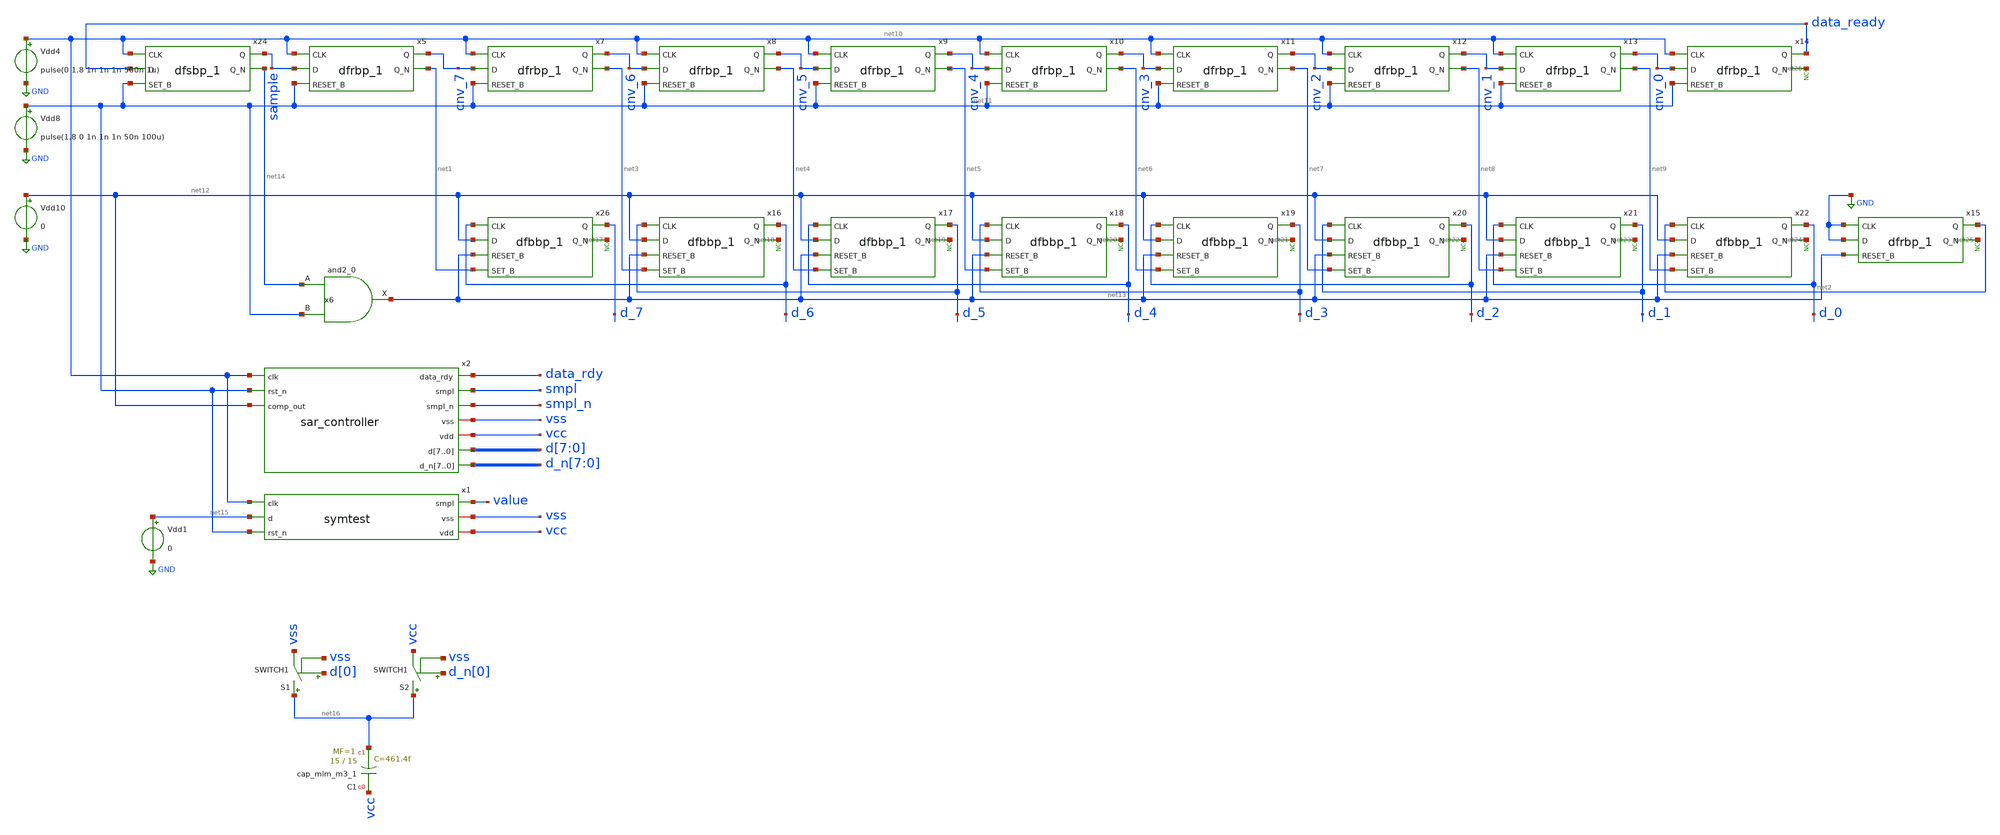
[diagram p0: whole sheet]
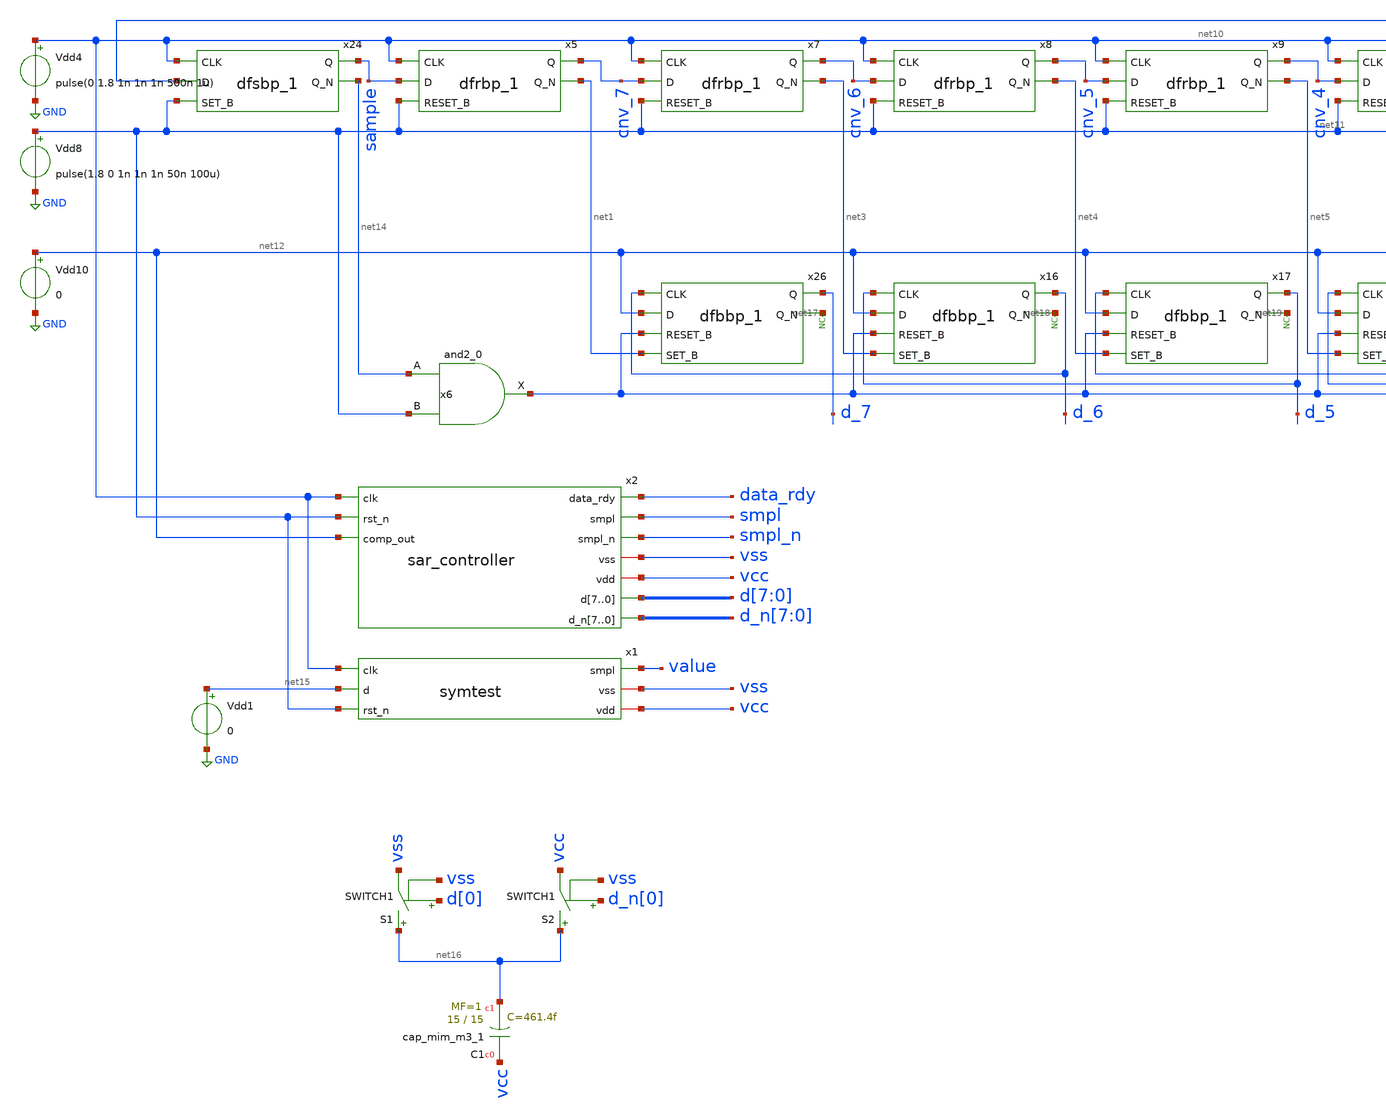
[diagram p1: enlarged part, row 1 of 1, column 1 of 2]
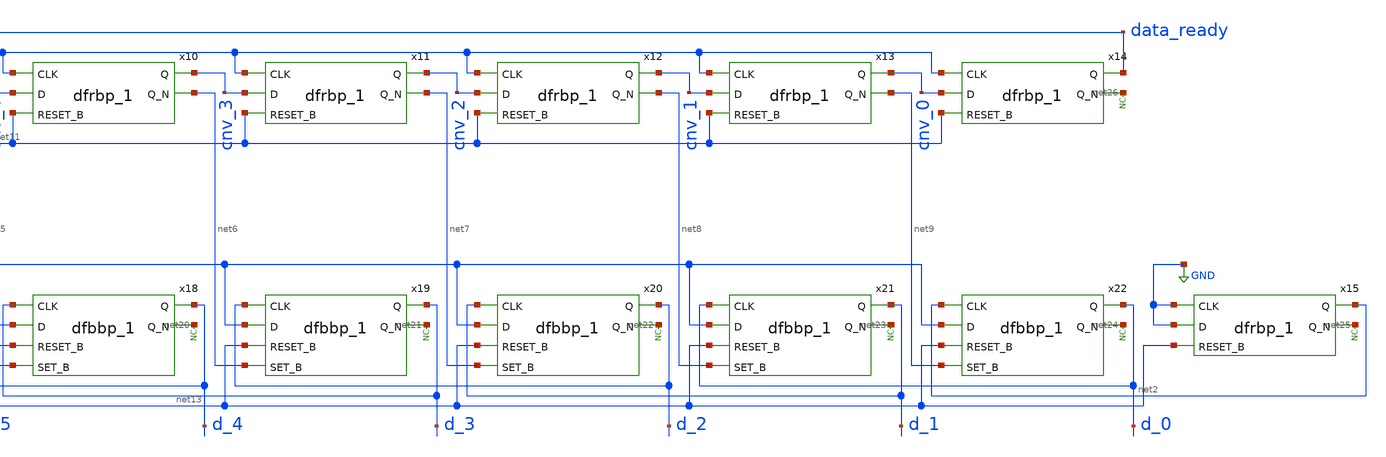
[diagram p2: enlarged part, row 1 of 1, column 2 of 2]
** sch_path: test/testbench/controller_tb.sch
.lib $::SKYWATER_MODELS/sky130.lib.spice tt
.include $::SKYWATER_STDCELLS/sky130_fd_sc_hd.spice

**.subckt controller_tb
x26 d_6 net12 net13 net1 vss vss vcc vcc d_7 net17 sky130_fd_sc_hd__dfbbp_1
x16 d_5 net12 net13 net3 vss vss vcc vcc d_6 net18 sky130_fd_sc_hd__dfbbp_1
x17 d_4 net12 net13 net4 vss vss vcc vcc d_5 net19 sky130_fd_sc_hd__dfbbp_1
x18 d_3 net12 net13 net5 vss vss vcc vcc d_4 net20 sky130_fd_sc_hd__dfbbp_1
x19 d_2 net12 net13 net6 vss vss vcc vcc d_3 net21 sky130_fd_sc_hd__dfbbp_1
x20 d_1 net12 net13 net7 vss vss vcc vcc d_2 net22 sky130_fd_sc_hd__dfbbp_1
x21 d_0 net12 net13 net8 vss vss vcc vcc d_1 net23 sky130_fd_sc_hd__dfbbp_1
x22 net2 net12 net13 net9 vss vss vcc vcc d_0 net24 sky130_fd_sc_hd__dfbbp_1
x5 net10 sample net11 vss vss vcc vcc cnv_7 net1 sky130_fd_sc_hd__dfrbp_1
Vdd10 net12 GND 0
Vdd8 net11 GND pulse(1.8 0 1n 1n 1n 50n 100u)
Vdd4 net10 GND pulse(0 1.8 1n 1n 1n 500n 1u)
* noconn #net17
* noconn #net18
* noconn #net19
* noconn #net20
* noconn #net21
* noconn #net22
* noconn #net23
* noconn #net24
* noconn #net25
x7 net10 cnv_7 net11 vss vss vcc vcc cnv_6 net3 sky130_fd_sc_hd__dfrbp_1
x8 net10 cnv_6 net11 vss vss vcc vcc cnv_5 net4 sky130_fd_sc_hd__dfrbp_1
x9 net10 cnv_5 net11 vss vss vcc vcc cnv_4 net5 sky130_fd_sc_hd__dfrbp_1
x10 net10 cnv_4 net11 vss vss vcc vcc cnv_3 net6 sky130_fd_sc_hd__dfrbp_1
x11 net10 cnv_3 net11 vss vss vcc vcc cnv_2 net7 sky130_fd_sc_hd__dfrbp_1
x12 net10 cnv_2 net11 vss vss vcc vcc cnv_1 net8 sky130_fd_sc_hd__dfrbp_1
x13 net10 cnv_1 net11 vss vss vcc vcc cnv_0 net9 sky130_fd_sc_hd__dfrbp_1
x14 net10 cnv_0 net11 vss vss vcc vcc data_ready net26 sky130_fd_sc_hd__dfrbp_1
* noconn #net26
x15 GND GND net13 vss vss vcc vcc net2 net25 sky130_fd_sc_hd__dfrbp_1
x24 net10 data_ready net11 vss vss vcc vcc sample net14 sky130_fd_sc_hd__dfsbp_1
x6 net14 net11 vss vss vcc vcc net13 sky130_fd_sc_hd__and2_0
x1 net10 value net15 net11 vss vcc symtest
Vdd1 net15 GND 0
x2 net10 data_rdy smpl net11 smpl_n net12 vss vcc d[7] d[6] d[5] d[4] d[3] d[2] d[1] d[0] d_n[7]
+ d_n[6] d_n[5] d_n[4] d_n[3] d_n[2] d_n[1] d_n[0] sar_controller
XC1 vcc net16 sky130_fd_pr__cap_mim_m3_1 W=15 L=15 MF=1 m=1
S2 net16 vcc d_n[0] vss SWITCH1
S1 net16 vss d[0] vss SWITCH1
**** begin user architecture code


.tran 10n 5u
.save all
.param vcc = 1.8
.param vdd = 1.8
vvcc vcc 0 dc vcc
vvdd vdd 0 dc vdd
vvss vss 0 0
.control

run

plot sample data_rdy

.endc



.model SWITCH1 sw vt=0.5 vh=0 ron=1 roff =1G

**** end user architecture code
**.ends
.GLOBAL GND
.end
